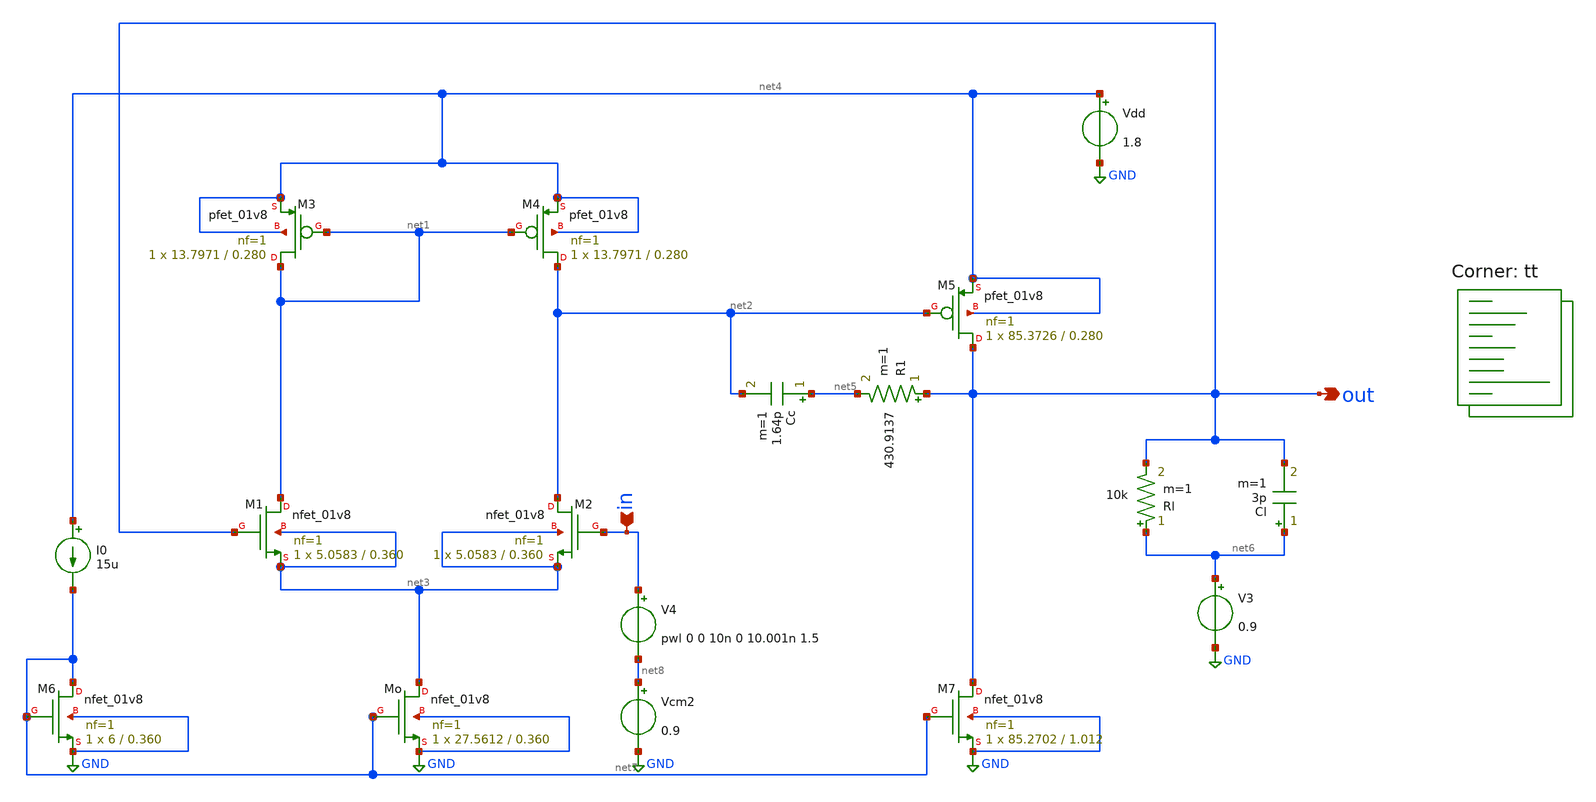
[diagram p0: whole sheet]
** sch_path: Design of 2-Stage OTA ,used in unity feedback/2-sTAGE_OTA_NMOS.sch
**.subckt 2-sTAGE_OTA_NMOS out in
*.opin out
*.ipin in
XM1 net1 out net3 net3 sky130_fd_pr__nfet_01v8 L=0.360 W=5.0583 nf=1 ad='int((nf+1)/2) * W/nf * 0.29'
+ as='int((nf+2)/2) * W/nf * 0.29' pd='2*int((nf+1)/2) * (W/nf + 0.29)' ps='2*int((nf+2)/2) * (W/nf + 0.29)'
+ nrd='0.29 / W' nrs='0.29 / W' sa=0 sb=0 sd=0 mult=1 m=1
XM2 net2 in net3 net3 sky130_fd_pr__nfet_01v8 L=0.360 W=5.0583 nf=1 ad='int((nf+1)/2) * W/nf * 0.29'
+ as='int((nf+2)/2) * W/nf * 0.29' pd='2*int((nf+1)/2) * (W/nf + 0.29)' ps='2*int((nf+2)/2) * (W/nf + 0.29)'
+ nrd='0.29 / W' nrs='0.29 / W' sa=0 sb=0 sd=0 mult=1 m=1
XM3 net1 net1 net4 net4 sky130_fd_pr__pfet_01v8 L=0.280 W=13.7971 nf=1 ad='int((nf+1)/2) * W/nf * 0.29'
+ as='int((nf+2)/2) * W/nf * 0.29' pd='2*int((nf+1)/2) * (W/nf + 0.29)' ps='2*int((nf+2)/2) * (W/nf + 0.29)'
+ nrd='0.29 / W' nrs='0.29 / W' sa=0 sb=0 sd=0 mult=1 m=1
XM4 net2 net1 net4 net4 sky130_fd_pr__pfet_01v8 L=0.280 W=13.7971 nf=1 ad='int((nf+1)/2) * W/nf * 0.29'
+ as='int((nf+2)/2) * W/nf * 0.29' pd='2*int((nf+1)/2) * (W/nf + 0.29)' ps='2*int((nf+2)/2) * (W/nf + 0.29)'
+ nrd='0.29 / W' nrs='0.29 / W' sa=0 sb=0 sd=0 mult=1 m=1
XM7 out net7 GND GND sky130_fd_pr__nfet_01v8 L=1.012 W=85.2702 nf=1 ad='int((nf+1)/2) * W/nf * 0.29'
+ as='int((nf+2)/2) * W/nf * 0.29' pd='2*int((nf+1)/2) * (W/nf + 0.29)' ps='2*int((nf+2)/2) * (W/nf + 0.29)'
+ nrd='0.29 / W' nrs='0.29 / W' sa=0 sb=0 sd=0 mult=1 m=1
Vdd net4 GND 1.8
Cc net5 net2 1.64p m=1
R1 out net5 430.9137 m=1
Cl net6 out 3p m=1
Rl net6 out 10k m=1
V3 net6 GND 0.9
XM5 out net2 net4 net4 sky130_fd_pr__pfet_01v8 L=0.280 W=85.3726 nf=1 ad='int((nf+1)/2) * W/nf * 0.29'
+ as='int((nf+2)/2) * W/nf * 0.29' pd='2*int((nf+1)/2) * (W/nf + 0.29)' ps='2*int((nf+2)/2) * (W/nf + 0.29)'
+ nrd='0.29 / W' nrs='0.29 / W' sa=0 sb=0 sd=0 mult=1 m=1
Vcm2 net8 GND 0.9
I0 net4 net7 15u
XM6 net7 net7 GND GND sky130_fd_pr__nfet_01v8 L=0.360 W=6 nf=1 ad='int((nf+1)/2) * W/nf * 0.29' as='int((nf+2)/2) * W/nf * 0.29'
+ pd='2*int((nf+1)/2) * (W/nf + 0.29)' ps='2*int((nf+2)/2) * (W/nf + 0.29)' nrd='0.29 / W' nrs='0.29 / W'
+ sa=0 sb=0 sd=0 mult=1 m=1
V4 in net8 pwl 0 0 10n 0 10.001n 1.5
XMo net3 net7 GND GND sky130_fd_pr__nfet_01v8 L=0.360 W=27.5612 nf=1 ad='int((nf+1)/2) * W/nf * 0.29'
+ as='int((nf+2)/2) * W/nf * 0.29' pd='2*int((nf+1)/2) * (W/nf + 0.29)' ps='2*int((nf+2)/2) * (W/nf + 0.29)'
+ nrd='0.29 / W' nrs='0.29 / W' sa=0 sb=0 sd=0 mult=1 m=1
**** begin user architecture code
.lib $::SKYWATER_MODELS/sky130.lib.spice tt


.option reltol=1e-5   abstol=1e-14 savecurrents
.option savecurrents
.control
*.print ac format=raw
save currents
save all
  save @m.xmo.msky130_fd_pr__nfet_01v8[vth]
  save @m.xmo.msky130_fd_pr__nfet_01v8[vgs]
  save @m.xmo.msky130_fd_pr__nfet_01v8[vds]
  save @m.xmo.msky130_fd_pr__nfet_01v8[gm]

  save @m.xm1.msky130_fd_pr__nfet_01v8[vth]
  save @m.xm1.msky130_fd_pr__nfet_01v8[vgs]
  save @m.xm1.msky130_fd_pr__nfet_01v8[vds]
  save @m.xm1.msky130_fd_pr__nfet_01v8[gm]

  save @m.xm2.msky130_fd_pr__nfet_01v8[vth]
  save @m.xm2.msky130_fd_pr__nfet_01v8[vgs]
  save @m.xm2.msky130_fd_pr__nfet_01v8[vds]
  save @m.xm2.msky130_fd_pr__nfet_01v8[gm]
  save @m.xm2.msky130_fd_pr__nfet_01v8[gds]

  save @m.xm3.msky130_fd_pr__pfet_01v8[vth]
  save @m.xm3.msky130_fd_pr__pfet_01v8[vgs]
  save @m.xm3.msky130_fd_pr__pfet_01v8[vds]
  save @m.xm3.msky130_fd_pr__pfet_01v8[gm]

  save @m.xm4.msky130_fd_pr__pfet_01v8[vth]
  save @m.xm4.msky130_fd_pr__pfet_01v8[vgs]
  save @m.xm4.msky130_fd_pr__pfet_01v8[vds]
  save @m.xm4.msky130_fd_pr__pfet_01v8[gm]
  save @m.xm4.msky130_fd_pr__pfet_01v8[gds]

  save @m.xm5.msky130_fd_pr__pfet_01v8[vth]
  save @m.xm5.msky130_fd_pr__pfet_01v8[vgs]
  save @m.xm5.msky130_fd_pr__pfet_01v8[vds]
  save @m.xm5.msky130_fd_pr__pfet_01v8[gm]

  save @m.xm6.msky130_fd_pr__nfet_01v8[vth]
  save @m.xm6.msky130_fd_pr__nfet_01v8[vgs]
  save @m.xm6.msky130_fd_pr__nfet_01v8[vds]
  save @m.xm6.msky130_fd_pr__nfet_01v8[gm]

  save @m.xm7.msky130_fd_pr__nfet_01v8[vth]
  save @m.xm7.msky130_fd_pr__nfet_01v8[vds]
  save @m.xm7.msky130_fd_pr__nfet_01v8[vgs]
  save @m.xm7.msky130_fd_pr__nfet_01v8[gm]
  op
  write 2-sTAGE_OTA_NMOS.raw
  *ac dec 10 0.1 1e8
  tran 1n  230n

  *set appendwrite
  *write 2-sTAGE_OTA_NMOS.raw
   *plot db(V(out)/V(in))
   *plot 180/pi*cph(V(out)/V(in))
    plot V(out)
.endc


**** end user architecture code
**.ends
.GLOBAL GND
.end
